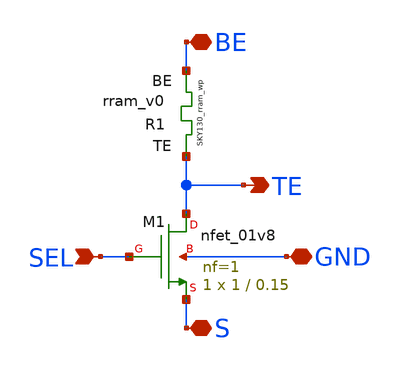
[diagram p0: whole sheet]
** sch_path: Ricardo/1T1R/1T1R_v2.sch
**.subckt 1T1R_v2 SEL BE S GND TE
*.ipin SEL
*.iopin BE
*.iopin S
*.iopin GND
*.opin TE
XR1 TE BE rram_v0
XM1 TE SEL S GND sky130_fd_pr__nfet_01v8 L=0.15 W=1 nf=1 ad='int((nf+1)/2) * W/nf * 0.29' as='int((nf+2)/2) * W/nf * 0.29'
+ pd='2*int((nf+1)/2) * (W/nf + 0.29)' ps='2*int((nf+2)/2) * (W/nf + 0.29)' nrd='0.29 / W' nrs='0.29 / W'
+ sa=0 sb=0 sd=0 mult=1 m=1
**.ends
.end
